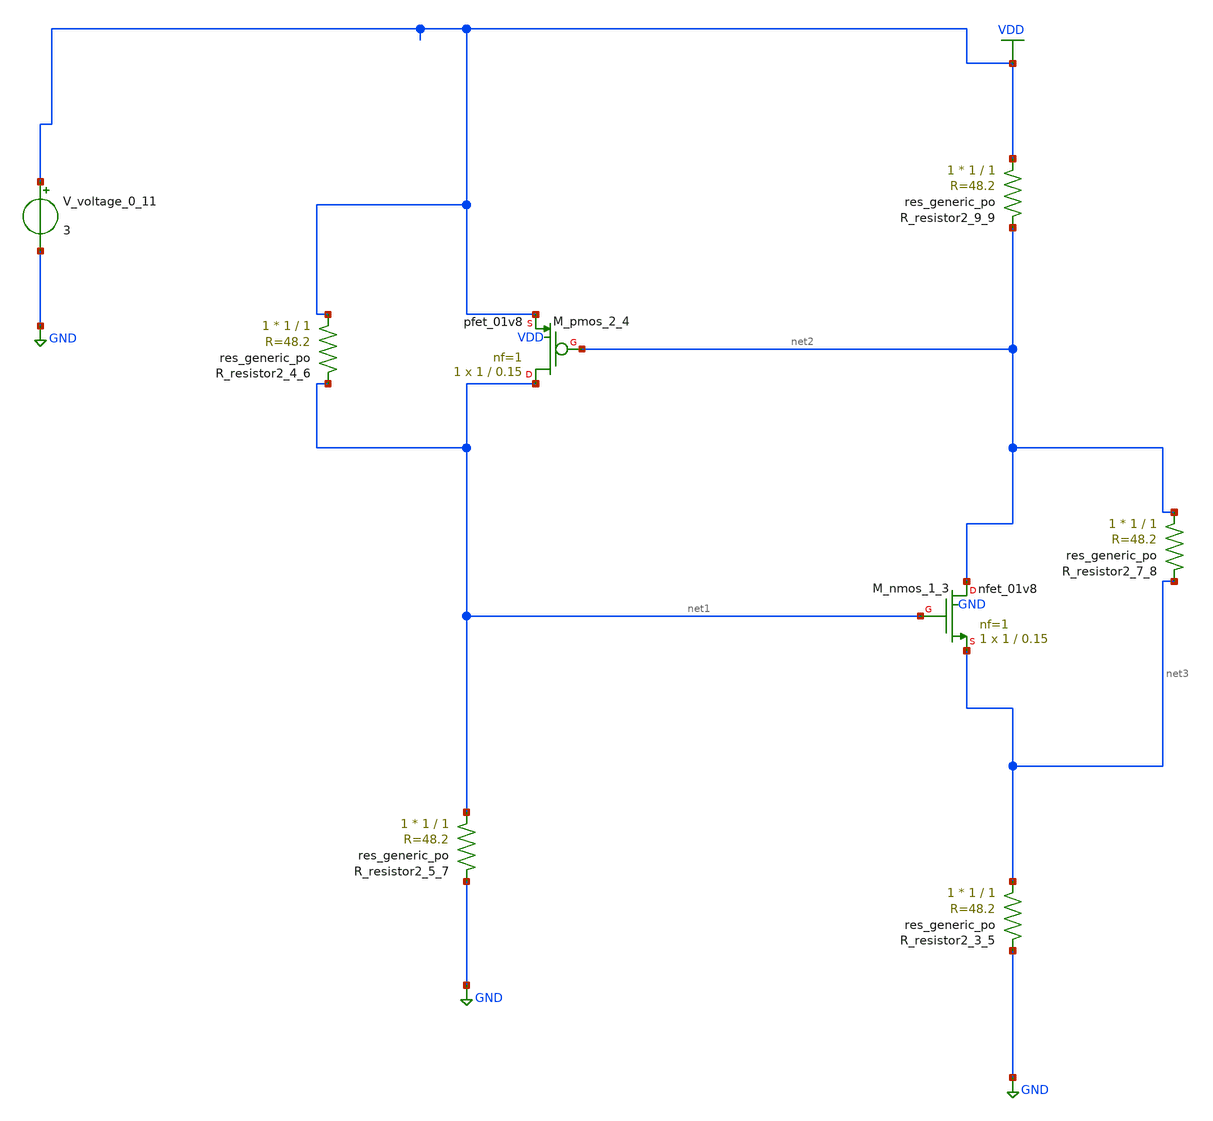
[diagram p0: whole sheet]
** sch_path: schematics/AMSNet/764.sch
**.subckt 764
XM_nmos_1_3 net2 net1 net3 GND sky130_fd_pr__nfet_01v8 L=0.15 W=1 nf=1 ad='int((1 + 1)/2) * 1 / 1 * 0.29'
+ as='int((1 + 2)/2) * 1 / 1 * 0.29' pd='2*int((1 + 1)/2) * (1 / 1 + 0.29)' ps='2*int((1 + 2)/2) * (1 / 1 + 0.29)'
+ nrd='0.29 / 1 ' nrs='0.29 / 1 ' sa=0 sb=0 sd=0 mult=1 m=1
XM_pmos_2_4 net1 net2 VDD VDD sky130_fd_pr__pfet_01v8 L=0.15 W=1 nf=1 ad='int((1 + 1)/2) * 1 / 1 * 0.29'
+ as='int((1 + 2)/2) * 1 / 1 * 0.29' pd='2*int((1 + 1)/2) * (1 / 1 + 0.29)' ps='2*int((1 + 2)/2) * (1 / 1 + 0.29)'
+ nrd='0.29 / 1 ' nrs='0.29 / 1 ' sa=0 sb=0 sd=0 mult=1 m=1
XR_resistor2_3_5 net3 GND sky130_fd_pr__res_generic_po W=1 L=1 m=1
XR_resistor2_4_6 VDD net1 sky130_fd_pr__res_generic_po W=1 L=1 m=1
XR_resistor2_5_7 net1 GND sky130_fd_pr__res_generic_po W=1 L=1 m=1
XR_resistor2_7_8 net2 net3 sky130_fd_pr__res_generic_po W=1 L=1 m=1
XR_resistor2_9_9 VDD net2 sky130_fd_pr__res_generic_po W=1 L=1 m=1
V_voltage_0_11 VDD GND 3
**.ends
.GLOBAL GND
.GLOBAL VDD
.end
